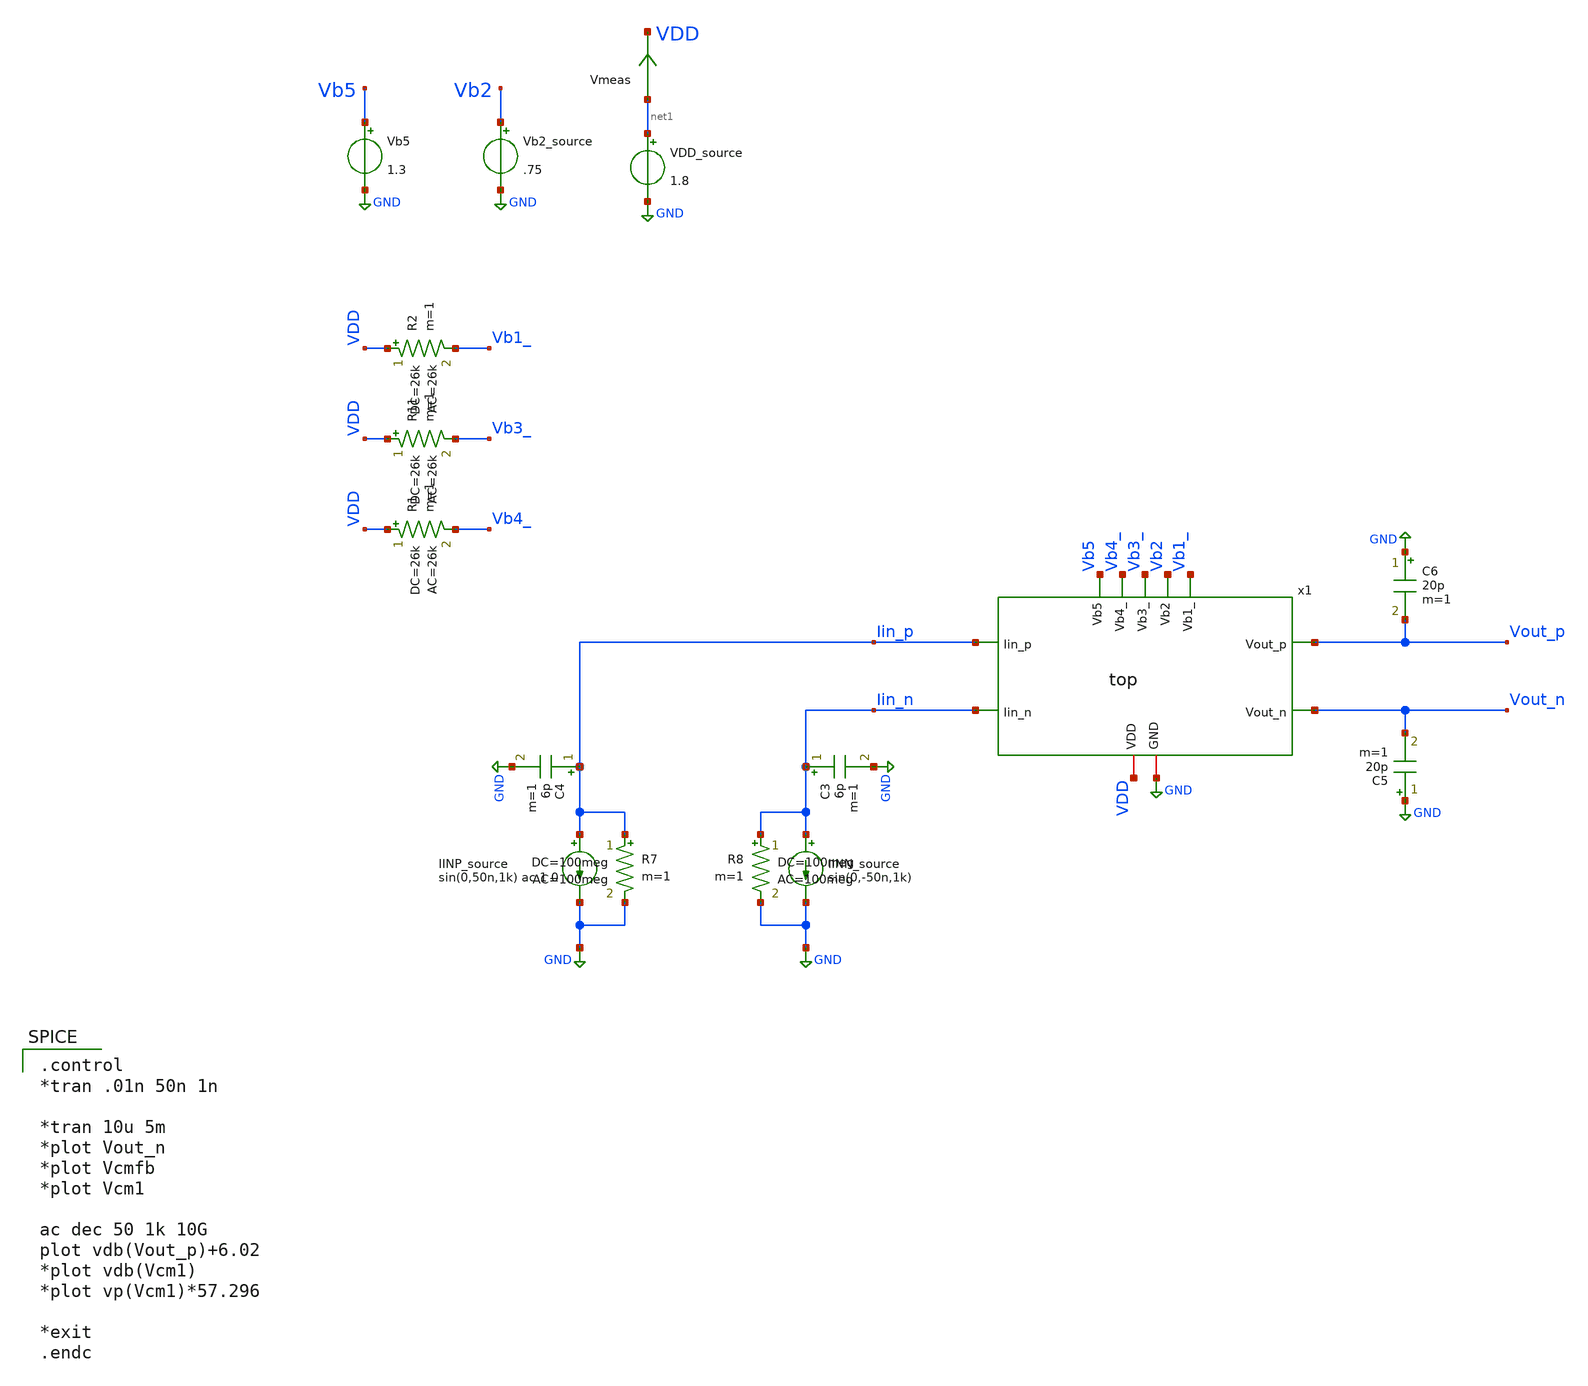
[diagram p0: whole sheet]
** sch_path: xschem/top_tb.sch
**.subckt top_tb
VDD_source net1 GND 1.8
Vmeas net1 VDD 0
.save i(vmeas)
Vb2_source Vb2 GND .75
C3 Iin_n GND 6p m=1
C4 Iin_p GND 6p m=1
IINP_source Iin_p GND sin(0,50n,1k) ac 1 0
IINN_source Iin_n GND sin(0,-50n,1k)
C5 GND Vout_n 20p m=1
C6 GND Vout_p 20p m=1
R7 Iin_p GND 100meg ac=100meg m=1
R8 Iin_n GND 100meg ac=100meg m=1
Vb5 Vb5 GND 1.3
R2 VDD Vb1_ 26k ac=26k m=1
R11 VDD Vb3_ 26k ac=26k m=1
x1 Iin_p Iin_n Vb1_ Vb2 Vb3_ Vb4_ Vb5 VDD GND Vout_n Vout_p top
R1 VDD Vb4_ 26k ac=26k m=1
**** begin user architecture code

.include $::SKYWATER_MODELS/cells/nfet_01v8/sky130_fd_pr__nfet_01v8__tt.corner.spice
.include $::SKYWATER_MODELS/cells/pfet_01v8/sky130_fd_pr__pfet_01v8__tt.corner.spice
.include $::SKYWATER_MODELS/cells/nfet_01v8_lvt/sky130_fd_pr__nfet_01v8_lvt__tt.corner.spice
*.include $::SKYWATER_MODELS/cells/nfet_03v3_nvt/sky130_fd_pr__nfet_03v3_nvt__tt.corner.spice
*.include $::SKYWATER_MODELS/cells/nfet_05v0_nvt/sky130_fd_pr__nfet_05v0_nvt__tt.corner.spice
*.include $::SKYWATER_MODELS/cells/esd_nfet_01v8/sky130_fd_pr__esd_nfet_01v8__tt.corner.spice
*.include $::SKYWATER_MODELS/cells/pfet_01v8_lvt/sky130_fd_pr__pfet_01v8_lvt__tt.corner.spice
*.include $::SKYWATER_MODELS/cells/pfet_01v8_hvt/sky130_fd_pr__pfet_01v8_hvt__tt.corner.spice
*.include $::SKYWATER_MODELS/models/corners/tt/nonfet.spice
* Mismatch parameters
.include $::SKYWATER_MODELS/cells/nfet_01v8/sky130_fd_pr__nfet_01v8__mismatch.corner.spice
.include $::SKYWATER_MODELS/cells/pfet_01v8/sky130_fd_pr__pfet_01v8__mismatch.corner.spice
.include $::SKYWATER_MODELS/cells/nfet_01v8_lvt/sky130_fd_pr__nfet_01v8_lvt__mismatch.corner.spice
*.include $::SKYWATER_MODELS/cells/pfet_01v8_lvt/sky130_fd_pr__pfet_01v8_lvt__mismatch.corner.spice
*.include $::SKYWATER_MODELS/cells/pfet_01v8_hvt/sky130_fd_pr__pfet_01v8_hvt__mismatch.corner.spice
*.include $::SKYWATER_MODELS/cells/nfet_g5v0d10v5/sky130_fd_pr__nfet_g5v0d10v5__mismatch.corner.spice
*.include $::SKYWATER_MODELS/cells/pfet_g5v0d10v5/sky130_fd_pr__pfet_g5v0d10v5__mismatch.corner.spice
*.include $::SKYWATER_MODELS/cells/nfet_05v0_nvt/sky130_fd_pr__nfet_05v0_nvt__mismatch.corner.spice
*.include $::SKYWATER_MODELS/cells/nfet_03v3_nvt/sky130_fd_pr__nfet_03v3_nvt__mismatch.corner.spice
* Resistor$::SKYWATER_MODELS/Capacitor
.include $::SKYWATER_MODELS/models/r+c/res_typical__cap_typical.spice
.include $::SKYWATER_MODELS/models/r+c/res_typical__cap_typical__lin.spice
* Special cells
*.include $::SKYWATER_MODELS/models/corners/tt/specialized_cells.spice
* All models
.include $::SKYWATER_MODELS/models/all.spice
* Corner
*.include $::SKYWATER_MODELS/models/corners/tt/rf.spice
.include /home/jared/Documents/GS_Design/tia_post_approval/pex/top_pex_fixed.spice


.option savecurrents
.control
save all
*NFET

save @m.xm90.msky130_fd_pr__nfet_01v8[vds] @m.xm90.msky130_fd_pr__nfet_01v8[gm]
+ @m.xm90.msky130_fd_pr__nfet_01v8[vth] @m.xm90.msky130_fd_pr__nfet_01v8[vgs] @m.xm90.msky130_fd_pr__nfet_01v8[id]
+ @m.xm90.msky130_fd_pr__nfet_01v8[gds] @m.xm90.msky130_fd_pr__nfet_01v8[cgg] @m.xm90.msky130_fd_pr__nfet_01v8[cgs]
+ @m.xm90.msky130_fd_pr__nfet_01v8[cgd] @m.xm90.msky130_fd_pr__nfet_01v8[cgb] @m.xm90.msky130_fd_pr__nfet_01v8[cdg]
+ @m.xm90.msky130_fd_pr__nfet_01v8[cds] @m.xm90.msky130_fd_pr__nfet_01v8[cdd] @m.xm90.msky130_fd_pr__nfet_01v8[cdb]
+ @m.xm90.msky130_fd_pr__nfet_01v8[csg] @m.xm90.msky130_fd_pr__nfet_01v8[css] @m.xm90.msky130_fd_pr__nfet_01v8[csd]
+ @m.xm90.msky130_fd_pr__nfet_01v8[csb] @m.xm90.msky130_fd_pr__nfet_01v8[cbg] @m.xm90.msky130_fd_pr__nfet_01v8[cbs]
+ @m.xm90.msky130_fd_pr__nfet_01v8[cbd] @m.xm90.msky130_fd_pr__nfet_01v8[cbb]
save @m.xm1.msky130_fd_pr__nfet_01v8[vds] @m.xm1.msky130_fd_pr__nfet_01v8[gm]
+ @m.xm1.msky130_fd_pr__nfet_01v8[vth] @m.xm1.msky130_fd_pr__nfet_01v8[vgs] @m.xm1.msky130_fd_pr__nfet_01v8[id]
+ @m.xm1.msky130_fd_pr__nfet_01v8[gds] @m.xm1.msky130_fd_pr__nfet_01v8[cgg] @m.xm1.msky130_fd_pr__nfet_01v8[cgs]
+ @m.xm1.msky130_fd_pr__nfet_01v8[cgd] @m.xm1.msky130_fd_pr__nfet_01v8[cgb] @m.xm1.msky130_fd_pr__nfet_01v8[cdg]
+ @m.xm1.msky130_fd_pr__nfet_01v8[cds] @m.xm1.msky130_fd_pr__nfet_01v8[cdd] @m.xm1.msky130_fd_pr__nfet_01v8[cdb]
+ @m.xm1.msky130_fd_pr__nfet_01v8[csg] @m.xm1.msky130_fd_pr__nfet_01v8[css] @m.xm1.msky130_fd_pr__nfet_01v8[csd]
+ @m.xm1.msky130_fd_pr__nfet_01v8[csb] @m.xm1.msky130_fd_pr__nfet_01v8[cbg] @m.xm1.msky130_fd_pr__nfet_01v8[cbs]
+ @m.xm1.msky130_fd_pr__nfet_01v8[cbd] @m.xm1.msky130_fd_pr__nfet_01v8[cbb]
save @m.xm2.msky130_fd_pr__nfet_01v8[vds] @m.xm2.msky130_fd_pr__nfet_01v8[gm]
+ @m.xm2.msky130_fd_pr__nfet_01v8[vth] @m.xm2.msky130_fd_pr__nfet_01v8[vgs] @m.xm2.msky130_fd_pr__nfet_01v8[id]
+ @m.xm2.msky130_fd_pr__nfet_01v8[gds] @m.xm2.msky130_fd_pr__nfet_01v8[cgg] @m.xm2.msky130_fd_pr__nfet_01v8[cgs]
+ @m.xm2.msky130_fd_pr__nfet_01v8[cgd] @m.xm2.msky130_fd_pr__nfet_01v8[cgb] @m.xm2.msky130_fd_pr__nfet_01v8[cdg]
+ @m.xm2.msky130_fd_pr__nfet_01v8[cds] @m.xm2.msky130_fd_pr__nfet_01v8[cdd] @m.xm2.msky130_fd_pr__nfet_01v8[cdb]
+ @m.xm2.msky130_fd_pr__nfet_01v8[csg] @m.xm2.msky130_fd_pr__nfet_01v8[css] @m.xm2.msky130_fd_pr__nfet_01v8[csd]
+ @m.xm2.msky130_fd_pr__nfet_01v8[csb] @m.xm2.msky130_fd_pr__nfet_01v8[cbg] @m.xm2.msky130_fd_pr__nfet_01v8[cbs]
+ @m.xm2.msky130_fd_pr__nfet_01v8[cbd] @m.xm2.msky130_fd_pr__nfet_01v8[cbb]
save @m.xm3.msky130_fd_pr__nfet_01v8[vds] @m.xm3.msky130_fd_pr__nfet_01v8[gm]
+ @m.xm3.msky130_fd_pr__nfet_01v8[vth] @m.xm3.msky130_fd_pr__nfet_01v8[vgs] @m.xm3.msky130_fd_pr__nfet_01v8[id]
+ @m.xm3.msky130_fd_pr__nfet_01v8[gds] @m.xm3.msky130_fd_pr__nfet_01v8[cgg] @m.xm3.msky130_fd_pr__nfet_01v8[cgs]
+ @m.xm3.msky130_fd_pr__nfet_01v8[cgd] @m.xm3.msky130_fd_pr__nfet_01v8[cgb] @m.xm3.msky130_fd_pr__nfet_01v8[cdg]
+ @m.xm3.msky130_fd_pr__nfet_01v8[cds] @m.xm3.msky130_fd_pr__nfet_01v8[cdd] @m.xm3.msky130_fd_pr__nfet_01v8[cdb]
+ @m.xm3.msky130_fd_pr__nfet_01v8[csg] @m.xm3.msky130_fd_pr__nfet_01v8[css] @m.xm3.msky130_fd_pr__nfet_01v8[csd]
+ @m.xm3.msky130_fd_pr__nfet_01v8[csb] @m.xm3.msky130_fd_pr__nfet_01v8[cbg] @m.xm3.msky130_fd_pr__nfet_01v8[cbs]
+ @m.xm3.msky130_fd_pr__nfet_01v8[cbd] @m.xm3.msky130_fd_pr__nfet_01v8[cbb]
save @m.xm6.msky130_fd_pr__nfet_01v8[vds] @m.xm6.msky130_fd_pr__nfet_01v8[gm]
+ @m.xm6.msky130_fd_pr__nfet_01v8[vth] @m.xm6.msky130_fd_pr__nfet_01v8[vgs] @m.xm6.msky130_fd_pr__nfet_01v8[id]
+ @m.xm6.msky130_fd_pr__nfet_01v8[gds] @m.xm6.msky130_fd_pr__nfet_01v8[cgg] @m.xm6.msky130_fd_pr__nfet_01v8[cgs]
+ @m.xm6.msky130_fd_pr__nfet_01v8[cgd] @m.xm6.msky130_fd_pr__nfet_01v8[cgb] @m.xm6.msky130_fd_pr__nfet_01v8[cdg]
+ @m.xm6.msky130_fd_pr__nfet_01v8[cds] @m.xm6.msky130_fd_pr__nfet_01v8[cdd] @m.xm6.msky130_fd_pr__nfet_01v8[cdb]
+ @m.xm6.msky130_fd_pr__nfet_01v8[csg] @m.xm6.msky130_fd_pr__nfet_01v8[css] @m.xm6.msky130_fd_pr__nfet_01v8[csd]
+ @m.xm6.msky130_fd_pr__nfet_01v8[csb] @m.xm6.msky130_fd_pr__nfet_01v8[cbg] @m.xm6.msky130_fd_pr__nfet_01v8[cbs]
+ @m.xm6.msky130_fd_pr__nfet_01v8[cbd] @m.xm6.msky130_fd_pr__nfet_01v8[cbb]
save @m.xm7.msky130_fd_pr__nfet_01v8[vds] @m.xm7.msky130_fd_pr__nfet_01v8[gm]
+ @m.xm7.msky130_fd_pr__nfet_01v8[vth] @m.xm7.msky130_fd_pr__nfet_01v8[vgs] @m.xm7.msky130_fd_pr__nfet_01v8[id]
+ @m.xm7.msky130_fd_pr__nfet_01v8[gds] @m.xm7.msky130_fd_pr__nfet_01v8[cgg] @m.xm7.msky130_fd_pr__nfet_01v8[cgs]
+ @m.xm7.msky130_fd_pr__nfet_01v8[cgd] @m.xm7.msky130_fd_pr__nfet_01v8[cgb] @m.xm7.msky130_fd_pr__nfet_01v8[cdg]
+ @m.xm7.msky130_fd_pr__nfet_01v8[cds] @m.xm7.msky130_fd_pr__nfet_01v8[cdd] @m.xm7.msky130_fd_pr__nfet_01v8[cdb]
+ @m.xm7.msky130_fd_pr__nfet_01v8[csg] @m.xm7.msky130_fd_pr__nfet_01v8[css] @m.xm7.msky130_fd_pr__nfet_01v8[csd]
+ @m.xm7.msky130_fd_pr__nfet_01v8[csb] @m.xm7.msky130_fd_pr__nfet_01v8[cbg] @m.xm7.msky130_fd_pr__nfet_01v8[cbs]
+ @m.xm7.msky130_fd_pr__nfet_01v8[cbd] @m.xm7.msky130_fd_pr__nfet_01v8[cbb]
save @m.xm8.msky130_fd_pr__nfet_01v8[vds] @m.xm8.msky130_fd_pr__nfet_01v8[gm]
+ @m.xm8.msky130_fd_pr__nfet_01v8[vth] @m.xm8.msky130_fd_pr__nfet_01v8[vgs] @m.xm8.msky130_fd_pr__nfet_01v8[id]
+ @m.xm8.msky130_fd_pr__nfet_01v8[gds] @m.xm8.msky130_fd_pr__nfet_01v8[cgg] @m.xm8.msky130_fd_pr__nfet_01v8[cgs]
+ @m.xm8.msky130_fd_pr__nfet_01v8[cgd] @m.xm8.msky130_fd_pr__nfet_01v8[cgb] @m.xm8.msky130_fd_pr__nfet_01v8[cdg]
+ @m.xm8.msky130_fd_pr__nfet_01v8[cds] @m.xm8.msky130_fd_pr__nfet_01v8[cdd] @m.xm8.msky130_fd_pr__nfet_01v8[cdb]
+ @m.xm8.msky130_fd_pr__nfet_01v8[csg] @m.xm8.msky130_fd_pr__nfet_01v8[css] @m.xm8.msky130_fd_pr__nfet_01v8[csd]
+ @m.xm8.msky130_fd_pr__nfet_01v8[csb] @m.xm8.msky130_fd_pr__nfet_01v8[cbg] @m.xm8.msky130_fd_pr__nfet_01v8[cbs]
+ @m.xm8.msky130_fd_pr__nfet_01v8[cbd] @m.xm8.msky130_fd_pr__nfet_01v8[cbb]
save @m.xm11.msky130_fd_pr__nfet_01v8[vds] @m.xm11.msky130_fd_pr__nfet_01v8[gm]
+ @m.xm11.msky130_fd_pr__nfet_01v8[vth] @m.xm11.msky130_fd_pr__nfet_01v8[vgs] @m.xm11.msky130_fd_pr__nfet_01v8[id]
+ @m.xm11.msky130_fd_pr__nfet_01v8[gds] @m.xm11.msky130_fd_pr__nfet_01v8[cgg] @m.xm11.msky130_fd_pr__nfet_01v8[cgs]
+ @m.xm11.msky130_fd_pr__nfet_01v8[cgd] @m.xm11.msky130_fd_pr__nfet_01v8[cgb] @m.xm11.msky130_fd_pr__nfet_01v8[cdg]
+ @m.xm11.msky130_fd_pr__nfet_01v8[cds] @m.xm11.msky130_fd_pr__nfet_01v8[cdd] @m.xm11.msky130_fd_pr__nfet_01v8[cdb]
+ @m.xm11.msky130_fd_pr__nfet_01v8[csg] @m.xm11.msky130_fd_pr__nfet_01v8[css] @m.xm11.msky130_fd_pr__nfet_01v8[csd]
+ @m.xm11.msky130_fd_pr__nfet_01v8[csb] @m.xm11.msky130_fd_pr__nfet_01v8[cbg] @m.xm11.msky130_fd_pr__nfet_01v8[cbs]
+ @m.xm11.msky130_fd_pr__nfet_01v8[cbd] @m.xm11.msky130_fd_pr__nfet_01v8[cbb]
save @m.xm12.msky130_fd_pr__nfet_01v8[vds] @m.xm12.msky130_fd_pr__nfet_01v8[gm]
+ @m.xm12.msky130_fd_pr__nfet_01v8[vth] @m.xm12.msky130_fd_pr__nfet_01v8[vgs] @m.xm12.msky130_fd_pr__nfet_01v8[id]
+ @m.xm12.msky130_fd_pr__nfet_01v8[gds] @m.xm12.msky130_fd_pr__nfet_01v8[cgg] @m.xm12.msky130_fd_pr__nfet_01v8[cgs]
+ @m.xm12.msky130_fd_pr__nfet_01v8[cgd] @m.xm12.msky130_fd_pr__nfet_01v8[cgb] @m.xm12.msky130_fd_pr__nfet_01v8[cdg]
+ @m.xm12.msky130_fd_pr__nfet_01v8[cds] @m.xm12.msky130_fd_pr__nfet_01v8[cdd] @m.xm12.msky130_fd_pr__nfet_01v8[cdb]
+ @m.xm12.msky130_fd_pr__nfet_01v8[csg] @m.xm12.msky130_fd_pr__nfet_01v8[css] @m.xm12.msky130_fd_pr__nfet_01v8[csd]
+ @m.xm12.msky130_fd_pr__nfet_01v8[csb] @m.xm12.msky130_fd_pr__nfet_01v8[cbg] @m.xm12.msky130_fd_pr__nfet_01v8[cbs]
+ @m.xm12.msky130_fd_pr__nfet_01v8[cbd] @m.xm12.msky130_fd_pr__nfet_01v8[cbb]
save @m.xm16.msky130_fd_pr__nfet_01v8[vds] @m.xm16.msky130_fd_pr__nfet_01v8[gm]
+ @m.xm16.msky130_fd_pr__nfet_01v8[vth] @m.xm16.msky130_fd_pr__nfet_01v8[vgs] @m.xm16.msky130_fd_pr__nfet_01v8[id]
+ @m.xm16.msky130_fd_pr__nfet_01v8[gds] @m.xm16.msky130_fd_pr__nfet_01v8[cgg] @m.xm16.msky130_fd_pr__nfet_01v8[cgs]
+ @m.xm16.msky130_fd_pr__nfet_01v8[cgd] @m.xm16.msky130_fd_pr__nfet_01v8[cgb] @m.xm16.msky130_fd_pr__nfet_01v8[cdg]
+ @m.xm16.msky130_fd_pr__nfet_01v8[cds] @m.xm16.msky130_fd_pr__nfet_01v8[cdd] @m.xm16.msky130_fd_pr__nfet_01v8[cdb]
+ @m.xm16.msky130_fd_pr__nfet_01v8[csg] @m.xm16.msky130_fd_pr__nfet_01v8[css] @m.xm16.msky130_fd_pr__nfet_01v8[csd]
+ @m.xm16.msky130_fd_pr__nfet_01v8[csb] @m.xm16.msky130_fd_pr__nfet_01v8[cbg] @m.xm16.msky130_fd_pr__nfet_01v8[cbs]
+ @m.xm16.msky130_fd_pr__nfet_01v8[cbd] @m.xm16.msky130_fd_pr__nfet_01v8[cbb]
save @m.xm17.msky130_fd_pr__nfet_01v8_lvt[vds] @m.xm17.msky130_fd_pr__nfet_01v8_lvt[gm]
+ @m.xm17.msky130_fd_pr__nfet_01v8_lvt[vth] @m.xm17.msky130_fd_pr__nfet_01v8_lvt[vgs] @m.xm17.msky130_fd_pr__nfet_01v8_lvt[id]
+ @m.xm17.msky130_fd_pr__nfet_01v8_lvt[gds] @m.xm17.msky130_fd_pr__nfet_01v8_lvt[cgg] @m.xm17.msky130_fd_pr__nfet_01v8_lvt[cgs]
+ @m.xm17.msky130_fd_pr__nfet_01v8_lvt[cgd] @m.xm17.msky130_fd_pr__nfet_01v8_lvt[cgb] @m.xm17.msky130_fd_pr__nfet_01v8_lvt[cdg]
+ @m.xm17.msky130_fd_pr__nfet_01v8_lvt[cds] @m.xm17.msky130_fd_pr__nfet_01v8_lvt[cdd] @m.xm17.msky130_fd_pr__nfet_01v8_lvt[cdb]
+ @m.xm17.msky130_fd_pr__nfet_01v8_lvt[csg] @m.xm17.msky130_fd_pr__nfet_01v8_lvt[css] @m.xm17.msky130_fd_pr__nfet_01v8_lvt[csd]
+ @m.xm17.msky130_fd_pr__nfet_01v8_lvt[csb] @m.xm17.msky130_fd_pr__nfet_01v8_lvt[cbg] @m.xm17.msky130_fd_pr__nfet_01v8_lvt[cbs]
+ @m.xm17.msky130_fd_pr__nfet_01v8_lvt[cbd] @m.xm17.msky130_fd_pr__nfet_01v8_lvt[cbb]
save @m.xm18.msky130_fd_pr__nfet_01v8_lvt[vds] @m.xm18.msky130_fd_pr__nfet_01v8_lvt[gm]
+ @m.xm18.msky130_fd_pr__nfet_01v8_lvt[vth] @m.xm18.msky130_fd_pr__nfet_01v8_lvt[vgs] @m.xm18.msky130_fd_pr__nfet_01v8_lvt[id]
+ @m.xm18.msky130_fd_pr__nfet_01v8_lvt[gds] @m.xm18.msky130_fd_pr__nfet_01v8_lvt[cgg] @m.xm18.msky130_fd_pr__nfet_01v8_lvt[cgs]
+ @m.xm18.msky130_fd_pr__nfet_01v8_lvt[cgd] @m.xm18.msky130_fd_pr__nfet_01v8_lvt[cgb] @m.xm18.msky130_fd_pr__nfet_01v8_lvt[cdg]
+ @m.xm18.msky130_fd_pr__nfet_01v8_lvt[cds] @m.xm18.msky130_fd_pr__nfet_01v8_lvt[cdd] @m.xm18.msky130_fd_pr__nfet_01v8_lvt[cdb]
+ @m.xm18.msky130_fd_pr__nfet_01v8_lvt[csg] @m.xm18.msky130_fd_pr__nfet_01v8_lvt[css] @m.xm18.msky130_fd_pr__nfet_01v8_lvt[csd]
+ @m.xm18.msky130_fd_pr__nfet_01v8_lvt[csb] @m.xm18.msky130_fd_pr__nfet_01v8_lvt[cbg] @m.xm18.msky130_fd_pr__nfet_01v8_lvt[cbs]
+ @m.xm18.msky130_fd_pr__nfet_01v8_lvt[cbd] @m.xm18.msky130_fd_pr__nfet_01v8_lvt[cbb]
save @m.xm19.msky130_fd_pr__nfet_01v8[vds] @m.xm19.msky130_fd_pr__nfet_01v8[gm]
+ @m.xm19.msky130_fd_pr__nfet_01v8[vth] @m.xm19.msky130_fd_pr__nfet_01v8[vgs] @m.xm19.msky130_fd_pr__nfet_01v8[id]
+ @m.xm19.msky130_fd_pr__nfet_01v8[gds] @m.xm19.msky130_fd_pr__nfet_01v8[cgg] @m.xm19.msky130_fd_pr__nfet_01v8[cgs]
+ @m.xm19.msky130_fd_pr__nfet_01v8[cgd] @m.xm19.msky130_fd_pr__nfet_01v8[cgb] @m.xm19.msky130_fd_pr__nfet_01v8[cdg]
+ @m.xm19.msky130_fd_pr__nfet_01v8[cds] @m.xm19.msky130_fd_pr__nfet_01v8[cdd] @m.xm19.msky130_fd_pr__nfet_01v8[cdb]
+ @m.xm19.msky130_fd_pr__nfet_01v8[csg] @m.xm19.msky130_fd_pr__nfet_01v8[css] @m.xm19.msky130_fd_pr__nfet_01v8[csd]
+ @m.xm19.msky130_fd_pr__nfet_01v8[csb] @m.xm19.msky130_fd_pr__nfet_01v8[cbg] @m.xm19.msky130_fd_pr__nfet_01v8[cbs]
+ @m.xm19.msky130_fd_pr__nfet_01v8[cbd] @m.xm19.msky130_fd_pr__nfet_01v8[cbb]
save @m.xm30.msky130_fd_pr__nfet_01v8[vds] @m.xm30.msky130_fd_pr__nfet_01v8[gm]
+ @m.xm30.msky130_fd_pr__nfet_01v8[vth] @m.xm30.msky130_fd_pr__nfet_01v8[vgs] @m.xm30.msky130_fd_pr__nfet_01v8[id]
+ @m.xm30.msky130_fd_pr__nfet_01v8[gds] @m.xm30.msky130_fd_pr__nfet_01v8[cgg] @m.xm30.msky130_fd_pr__nfet_01v8[cgs]
+ @m.xm30.msky130_fd_pr__nfet_01v8[cgd] @m.xm30.msky130_fd_pr__nfet_01v8[cgb] @m.xm30.msky130_fd_pr__nfet_01v8[cdg]
+ @m.xm30.msky130_fd_pr__nfet_01v8[cds] @m.xm30.msky130_fd_pr__nfet_01v8[cdd] @m.xm30.msky130_fd_pr__nfet_01v8[cdb]
+ @m.xm30.msky130_fd_pr__nfet_01v8[csg] @m.xm30.msky130_fd_pr__nfet_01v8[css] @m.xm30.msky130_fd_pr__nfet_01v8[csd]
+ @m.xm30.msky130_fd_pr__nfet_01v8[csb] @m.xm30.msky130_fd_pr__nfet_01v8[cbg] @m.xm30.msky130_fd_pr__nfet_01v8[cbs]
+ @m.xm30.msky130_fd_pr__nfet_01v8[cbd] @m.xm30.msky130_fd_pr__nfet_01v8[cbb]
save @m.xm26.msky130_fd_pr__nfet_01v8[vds] @m.xm26.msky130_fd_pr__nfet_01v8[gm]
+ @m.xm26.msky130_fd_pr__nfet_01v8[vth] @m.xm26.msky130_fd_pr__nfet_01v8[vgs] @m.xm26.msky130_fd_pr__nfet_01v8[id]
+ @m.xm26.msky130_fd_pr__nfet_01v8[gds] @m.xm26.msky130_fd_pr__nfet_01v8[cgg] @m.xm26.msky130_fd_pr__nfet_01v8[cgs]
+ @m.xm26.msky130_fd_pr__nfet_01v8[cgd] @m.xm26.msky130_fd_pr__nfet_01v8[cgb] @m.xm26.msky130_fd_pr__nfet_01v8[cdg]
+ @m.xm26.msky130_fd_pr__nfet_01v8[cds] @m.xm26.msky130_fd_pr__nfet_01v8[cdd] @m.xm26.msky130_fd_pr__nfet_01v8[cdb]
+ @m.xm26.msky130_fd_pr__nfet_01v8[csg] @m.xm26.msky130_fd_pr__nfet_01v8[css] @m.xm26.msky130_fd_pr__nfet_01v8[csd]
+ @m.xm26.msky130_fd_pr__nfet_01v8[csb] @m.xm26.msky130_fd_pr__nfet_01v8[cbg] @m.xm26.msky130_fd_pr__nfet_01v8[cbs]
+ @m.xm26.msky130_fd_pr__nfet_01v8[cbd] @m.xm26.msky130_fd_pr__nfet_01v8[cbb]
save @m.xm27.msky130_fd_pr__nfet_01v8[vds] @m.xm27.msky130_fd_pr__nfet_01v8[gm]
+ @m.xm27.msky130_fd_pr__nfet_01v8[vth] @m.xm27.msky130_fd_pr__nfet_01v8[vgs] @m.xm27.msky130_fd_pr__nfet_01v8[id]
+ @m.xm27.msky130_fd_pr__nfet_01v8[gds] @m.xm27.msky130_fd_pr__nfet_01v8[cgg] @m.xm27.msky130_fd_pr__nfet_01v8[cgs]
+ @m.xm27.msky130_fd_pr__nfet_01v8[cgd] @m.xm27.msky130_fd_pr__nfet_01v8[cgb] @m.xm27.msky130_fd_pr__nfet_01v8[cdg]
+ @m.xm27.msky130_fd_pr__nfet_01v8[cds] @m.xm27.msky130_fd_pr__nfet_01v8[cdd] @m.xm27.msky130_fd_pr__nfet_01v8[cdb]
+ @m.xm27.msky130_fd_pr__nfet_01v8[csg] @m.xm27.msky130_fd_pr__nfet_01v8[css] @m.xm27.msky130_fd_pr__nfet_01v8[csd]
+ @m.xm27.msky130_fd_pr__nfet_01v8[csb] @m.xm27.msky130_fd_pr__nfet_01v8[cbg] @m.xm27.msky130_fd_pr__nfet_01v8[cbs]
+ @m.xm27.msky130_fd_pr__nfet_01v8[cbd] @m.xm27.msky130_fd_pr__nfet_01v8[cbb]

*PFET

save @m.xm91.msky130_fd_pr__pfet_01v8[vds] @m.xm91.msky130_fd_pr__pfet_01v8[gm]
+ @m.xm91.msky130_fd_pr__pfet_01v8[vth] @m.xm91.msky130_fd_pr__pfet_01v8[vgs] @m.xm91.msky130_fd_pr__pfet_01v8[id]
+ @m.xm91.msky130_fd_pr__pfet_01v8[gds] @m.xm91.msky130_fd_pr__pfet_01v8[cgg] @m.xm91.msky130_fd_pr__pfet_01v8[cgs]
+ @m.xm91.msky130_fd_pr__pfet_01v8[cgd] @m.xm91.msky130_fd_pr__pfet_01v8[cgb] @m.xm91.msky130_fd_pr__pfet_01v8[cdg]
+ @m.xm91.msky130_fd_pr__pfet_01v8[cds] @m.xm91.msky130_fd_pr__pfet_01v8[cdd] @m.xm91.msky130_fd_pr__pfet_01v8[cdb]
+ @m.xm91.msky130_fd_pr__pfet_01v8[csg] @m.xm91.msky130_fd_pr__pfet_01v8[css] @m.xm91.msky130_fd_pr__pfet_01v8[csd]
+ @m.xm91.msky130_fd_pr__pfet_01v8[csb] @m.xm91.msky130_fd_pr__pfet_01v8[cbg] @m.xm91.msky130_fd_pr__pfet_01v8[cbs]
+ @m.xm91.msky130_fd_pr__pfet_01v8[cbd] @m.xm91.msky130_fd_pr__pfet_01v8[cbb]
save @m.xm4.msky130_fd_pr__pfet_01v8[vds] @m.xm4.msky130_fd_pr__pfet_01v8[gm]
+ @m.xm4.msky130_fd_pr__pfet_01v8[vth] @m.xm4.msky130_fd_pr__pfet_01v8[vgs] @m.xm4.msky130_fd_pr__pfet_01v8[id]
+ @m.xm4.msky130_fd_pr__pfet_01v8[gds] @m.xm4.msky130_fd_pr__pfet_01v8[cgg] @m.xm4.msky130_fd_pr__pfet_01v8[cgs]
+ @m.xm4.msky130_fd_pr__pfet_01v8[cgd] @m.xm4.msky130_fd_pr__pfet_01v8[cgb] @m.xm4.msky130_fd_pr__pfet_01v8[cdg]
+ @m.xm4.msky130_fd_pr__pfet_01v8[cds] @m.xm4.msky130_fd_pr__pfet_01v8[cdd] @m.xm4.msky130_fd_pr__pfet_01v8[cdb]
+ @m.xm4.msky130_fd_pr__pfet_01v8[csg] @m.xm4.msky130_fd_pr__pfet_01v8[css] @m.xm4.msky130_fd_pr__pfet_01v8[csd]
+ @m.xm4.msky130_fd_pr__pfet_01v8[csb] @m.xm4.msky130_fd_pr__pfet_01v8[cbg] @m.xm4.msky130_fd_pr__pfet_01v8[cbs]
+ @m.xm4.msky130_fd_pr__pfet_01v8[cbd] @m.xm4.msky130_fd_pr__pfet_01v8[cbb]
save @m.xm5.msky130_fd_pr__pfet_01v8[vds] @m.xm5.msky130_fd_pr__pfet_01v8[gm]
+ @m.xm5.msky130_fd_pr__pfet_01v8[vth] @m.xm5.msky130_fd_pr__pfet_01v8[vgs] @m.xm5.msky130_fd_pr__pfet_01v8[id]
+ @m.xm5.msky130_fd_pr__pfet_01v8[gds] @m.xm5.msky130_fd_pr__pfet_01v8[cgg] @m.xm5.msky130_fd_pr__pfet_01v8[cgs]
+ @m.xm5.msky130_fd_pr__pfet_01v8[cgd] @m.xm5.msky130_fd_pr__pfet_01v8[cgb] @m.xm5.msky130_fd_pr__pfet_01v8[cdg]
+ @m.xm5.msky130_fd_pr__pfet_01v8[cds] @m.xm5.msky130_fd_pr__pfet_01v8[cdd] @m.xm5.msky130_fd_pr__pfet_01v8[cdb]
+ @m.xm5.msky130_fd_pr__pfet_01v8[csg] @m.xm5.msky130_fd_pr__pfet_01v8[css] @m.xm5.msky130_fd_pr__pfet_01v8[csd]
+ @m.xm5.msky130_fd_pr__pfet_01v8[csb] @m.xm5.msky130_fd_pr__pfet_01v8[cbg] @m.xm5.msky130_fd_pr__pfet_01v8[cbs]
+ @m.xm5.msky130_fd_pr__pfet_01v8[cbd] @m.xm5.msky130_fd_pr__pfet_01v8[cbb]
save @m.xm9.msky130_fd_pr__pfet_01v8[vds] @m.xm9.msky130_fd_pr__pfet_01v8[gm]
+ @m.xm9.msky130_fd_pr__pfet_01v8[vth] @m.xm9.msky130_fd_pr__pfet_01v8[vgs] @m.xm9.msky130_fd_pr__pfet_01v8[id]
+ @m.xm9.msky130_fd_pr__pfet_01v8[gds] @m.xm9.msky130_fd_pr__pfet_01v8[cgg] @m.xm9.msky130_fd_pr__pfet_01v8[cgs]
+ @m.xm9.msky130_fd_pr__pfet_01v8[cgd] @m.xm9.msky130_fd_pr__pfet_01v8[cgb] @m.xm9.msky130_fd_pr__pfet_01v8[cdg]
+ @m.xm9.msky130_fd_pr__pfet_01v8[cds] @m.xm9.msky130_fd_pr__pfet_01v8[cdd] @m.xm9.msky130_fd_pr__pfet_01v8[cdb]
+ @m.xm9.msky130_fd_pr__pfet_01v8[csg] @m.xm9.msky130_fd_pr__pfet_01v8[css] @m.xm9.msky130_fd_pr__pfet_01v8[csd]
+ @m.xm9.msky130_fd_pr__pfet_01v8[csb] @m.xm9.msky130_fd_pr__pfet_01v8[cbg] @m.xm9.msky130_fd_pr__pfet_01v8[cbs]
+ @m.xm9.msky130_fd_pr__pfet_01v8[cbd] @m.xm9.msky130_fd_pr__pfet_01v8[cbb]
save @m.xm10.msky130_fd_pr__pfet_01v8[vds] @m.xm10.msky130_fd_pr__pfet_01v8[gm]
+ @m.xm10.msky130_fd_pr__pfet_01v8[vth] @m.xm10.msky130_fd_pr__pfet_01v8[vgs] @m.xm10.msky130_fd_pr__pfet_01v8[id]
+ @m.xm10.msky130_fd_pr__pfet_01v8[gds] @m.xm10.msky130_fd_pr__pfet_01v8[cgg] @m.xm10.msky130_fd_pr__pfet_01v8[cgs]
+ @m.xm10.msky130_fd_pr__pfet_01v8[cgd] @m.xm10.msky130_fd_pr__pfet_01v8[cgb] @m.xm10.msky130_fd_pr__pfet_01v8[cdg]
+ @m.xm10.msky130_fd_pr__pfet_01v8[cds] @m.xm10.msky130_fd_pr__pfet_01v8[cdd] @m.xm10.msky130_fd_pr__pfet_01v8[cdb]
+ @m.xm10.msky130_fd_pr__pfet_01v8[csg] @m.xm10.msky130_fd_pr__pfet_01v8[css] @m.xm10.msky130_fd_pr__pfet_01v8[csd]
+ @m.xm10.msky130_fd_pr__pfet_01v8[csb] @m.xm10.msky130_fd_pr__pfet_01v8[cbg] @m.xm10.msky130_fd_pr__pfet_01v8[cbs]
+ @m.xm10.msky130_fd_pr__pfet_01v8[cbd] @m.xm10.msky130_fd_pr__pfet_01v8[cbb]
save @m.xm13.msky130_fd_pr__pfet_01v8[vds] @m.xm13.msky130_fd_pr__pfet_01v8[gm]
+ @m.xm13.msky130_fd_pr__pfet_01v8[vth] @m.xm13.msky130_fd_pr__pfet_01v8[vgs] @m.xm13.msky130_fd_pr__pfet_01v8[id]
+ @m.xm13.msky130_fd_pr__pfet_01v8[gds] @m.xm13.msky130_fd_pr__pfet_01v8[cgg] @m.xm13.msky130_fd_pr__pfet_01v8[cgs]
+ @m.xm13.msky130_fd_pr__pfet_01v8[cgd] @m.xm13.msky130_fd_pr__pfet_01v8[cgb] @m.xm13.msky130_fd_pr__pfet_01v8[cdg]
+ @m.xm13.msky130_fd_pr__pfet_01v8[cds] @m.xm13.msky130_fd_pr__pfet_01v8[cdd] @m.xm13.msky130_fd_pr__pfet_01v8[cdb]
+ @m.xm13.msky130_fd_pr__pfet_01v8[csg] @m.xm13.msky130_fd_pr__pfet_01v8[css] @m.xm13.msky130_fd_pr__pfet_01v8[csd]
+ @m.xm13.msky130_fd_pr__pfet_01v8[csb] @m.xm13.msky130_fd_pr__pfet_01v8[cbg] @m.xm13.msky130_fd_pr__pfet_01v8[cbs]
+ @m.xm13.msky130_fd_pr__pfet_01v8[cbd] @m.xm13.msky130_fd_pr__pfet_01v8[cbb]
save @m.xm14.msky130_fd_pr__pfet_01v8[vds] @m.xm14.msky130_fd_pr__pfet_01v8[gm]
+ @m.xm14.msky130_fd_pr__pfet_01v8[vth] @m.xm14.msky130_fd_pr__pfet_01v8[vgs] @m.xm14.msky130_fd_pr__pfet_01v8[id]
+ @m.xm14.msky130_fd_pr__pfet_01v8[gds] @m.xm14.msky130_fd_pr__pfet_01v8[cgg] @m.xm14.msky130_fd_pr__pfet_01v8[cgs]
+ @m.xm14.msky130_fd_pr__pfet_01v8[cgd] @m.xm14.msky130_fd_pr__pfet_01v8[cgb] @m.xm14.msky130_fd_pr__pfet_01v8[cdg]
+ @m.xm14.msky130_fd_pr__pfet_01v8[cds] @m.xm14.msky130_fd_pr__pfet_01v8[cdd] @m.xm14.msky130_fd_pr__pfet_01v8[cdb]
+ @m.xm14.msky130_fd_pr__pfet_01v8[csg] @m.xm14.msky130_fd_pr__pfet_01v8[css] @m.xm14.msky130_fd_pr__pfet_01v8[csd]
+ @m.xm14.msky130_fd_pr__pfet_01v8[csb] @m.xm14.msky130_fd_pr__pfet_01v8[cbg] @m.xm14.msky130_fd_pr__pfet_01v8[cbs]
+ @m.xm14.msky130_fd_pr__pfet_01v8[cbd] @m.xm14.msky130_fd_pr__pfet_01v8[cbb]
save @m.xm24.msky130_fd_pr__pfet_01v8[vds] @m.xm24.msky130_fd_pr__pfet_01v8[gm]
+ @m.xm24.msky130_fd_pr__pfet_01v8[vth] @m.xm24.msky130_fd_pr__pfet_01v8[vgs] @m.xm24.msky130_fd_pr__pfet_01v8[id]
+ @m.xm24.msky130_fd_pr__pfet_01v8[gds] @m.xm24.msky130_fd_pr__pfet_01v8[cgg] @m.xm24.msky130_fd_pr__pfet_01v8[cgs]
+ @m.xm24.msky130_fd_pr__pfet_01v8[cgd] @m.xm24.msky130_fd_pr__pfet_01v8[cgb] @m.xm24.msky130_fd_pr__pfet_01v8[cdg]
+ @m.xm24.msky130_fd_pr__pfet_01v8[cds] @m.xm24.msky130_fd_pr__pfet_01v8[cdd] @m.xm24.msky130_fd_pr__pfet_01v8[cdb]
+ @m.xm24.msky130_fd_pr__pfet_01v8[csg] @m.xm24.msky130_fd_pr__pfet_01v8[css] @m.xm24.msky130_fd_pr__pfet_01v8[csd]
+ @m.xm24.msky130_fd_pr__pfet_01v8[csb] @m.xm24.msky130_fd_pr__pfet_01v8[cbg] @m.xm24.msky130_fd_pr__pfet_01v8[cbs]
+ @m.xm24.msky130_fd_pr__pfet_01v8[cbd] @m.xm24.msky130_fd_pr__pfet_01v8[cbb]
save @m.xm25.msky130_fd_pr__pfet_01v8[vds] @m.xm25.msky130_fd_pr__pfet_01v8[gm]
+ @m.xm25.msky130_fd_pr__pfet_01v8[vth] @m.xm25.msky130_fd_pr__pfet_01v8[vgs] @m.xm25.msky130_fd_pr__pfet_01v8[id]
+ @m.xm25.msky130_fd_pr__pfet_01v8[gds] @m.xm25.msky130_fd_pr__pfet_01v8[cgg] @m.xm25.msky130_fd_pr__pfet_01v8[cgs]
+ @m.xm25.msky130_fd_pr__pfet_01v8[cgd] @m.xm25.msky130_fd_pr__pfet_01v8[cgb] @m.xm25.msky130_fd_pr__pfet_01v8[cdg]
+ @m.xm25.msky130_fd_pr__pfet_01v8[cds] @m.xm25.msky130_fd_pr__pfet_01v8[cdd] @m.xm25.msky130_fd_pr__pfet_01v8[cdb]
+ @m.xm25.msky130_fd_pr__pfet_01v8[csg] @m.xm25.msky130_fd_pr__pfet_01v8[css] @m.xm25.msky130_fd_pr__pfet_01v8[csd]
+ @m.xm25.msky130_fd_pr__pfet_01v8[csb] @m.xm25.msky130_fd_pr__pfet_01v8[cbg] @m.xm25.msky130_fd_pr__pfet_01v8[cbs]
+ @m.xm25.msky130_fd_pr__pfet_01v8[cbd] @m.xm25.msky130_fd_pr__pfet_01v8[cbb]

op
write top_tb.raw
.endc


.control
*tran .01n 50n 1n

*tran 10u 5m
*plot Vout_n
*plot Vcmfb
*plot Vcm1

ac dec 50 1k 10G
plot vdb(Vout_p)+6.02
*plot vdb(Vcm1)
*plot vp(Vcm1)*57.296

*exit
.endc


**** end user architecture code
**.ends

* expanding   symbol:  tia_post_approval/schem/top.sym # of pins=11
** sym_path: tia_post_approval/schem/top.sym
** sch_path: tia_post_approval/schem/top.sch
.subckt top Iin_p Iin_n Vb1_ Vb2 Vb3_ Vb4_ Vb5 VDD GND Vout_n Vout_p
*.iopin VDD
*.iopin GND
*.opin Vout_n
*.ipin Iin_n
*.ipin Iin_p
*.ipin Vb1_
*.opin Vout_p
*.ipin Vb2
*.ipin Vb3_
*.ipin Vb4_
*.ipin Vb5
XR6 Vinn pre_Vout_p GND sky130_fd_pr__res_xhigh_po W=1.41 L=53 mult=1 m=1
XR1 pre_Vout_n Vinp GND sky130_fd_pr__res_xhigh_po W=1.41 L=53 mult=1 m=1
XR3 Vcm2 pre_Vout_p GND sky130_fd_pr__res_xhigh_po W=1.41 L=35 mult=1 m=1
XR5 pre_Vout_n Vcm2 GND sky130_fd_pr__res_xhigh_po W=1.41 L=35 mult=1 m=1
XR4 Vop net1 GND sky130_fd_pr__res_xhigh_po W=1.41 L=1.41 mult=1 m=1
XR10 Von net2 GND sky130_fd_pr__res_xhigh_po W=1.41 L=1.41 mult=1 m=1
XR17 Vcm1 Von GND sky130_fd_pr__res_xhigh_po W=1.41 L=35 mult=1 m=1
XR18 Vop Vcm1 GND sky130_fd_pr__res_xhigh_po W=1.41 L=35 mult=1 m=1
x1 Vinn Vinp Vb2 Vb1 Vcmfb1 VDD GND Vop Von core
x2 Vop Von Vb2 Vb1 Vcmfb2 VDD GND pre_Vout_n pre_Vout_p core
X1 VDD GND pre_Vout_n pre_Vout_p Vout_n Vout_p Vb4 sf
x3 Vcm1 Vb5 Vb3 VDD GND Vcmfb1 cmfb
x4 Vcm2 Vb5 Vb3 VDD GND Vcmfb2 cmfb
x5 Vb1 Vb1_ GND mirror_1
x6 Vb3 Vb3_ GND mirror_3
x7 Vb4 Vb4_ GND mirror_4
XC3 net1 pre_Vout_n sky130_fd_pr__cap_mim_m3_1 W=7.75 L=7.75 MF=1 m=1
XC4 pre_Vout_n net1 sky130_fd_pr__cap_mim_m3_2 W=7.75 L=7.75 MF=1 m=1
XC1 net2 pre_Vout_p sky130_fd_pr__cap_mim_m3_1 W=7.75 L=7.75 MF=1 m=1
XC2 pre_Vout_p net2 sky130_fd_pr__cap_mim_m3_2 W=7.75 L=7.75 MF=1 m=1
XC5 Vinn Iin_n sky130_fd_pr__cap_mim_m3_1 W=61.2 L=61.2 MF=1 m=1
XC6 Iin_n Vinn sky130_fd_pr__cap_mim_m3_2 W=61.2 L=61.2 MF=1 m=1
XC7 Vinp Iin_p sky130_fd_pr__cap_mim_m3_1 W=61.2 L=61.2 MF=1 m=1
XC8 Iin_p Vinp sky130_fd_pr__cap_mim_m3_2 W=61.2 L=61.2 MF=1 m=1
XC9 Vcmfb1 GND sky130_fd_pr__cap_mim_m3_1 W=33.5 L=33.5 MF=1 m=1
XC10 GND Vcmfb1 sky130_fd_pr__cap_mim_m3_2 W=33.5 L=33.5 MF=1 m=1
XC11 Vcmfb2 GND sky130_fd_pr__cap_mim_m3_1 W=33.5 L=33.5 MF=1 m=1
XC12 GND Vcmfb2 sky130_fd_pr__cap_mim_m3_2 W=33.5 L=33.5 MF=1 m=1
.ends


* expanding   symbol:  tia_post_approval/schem/core.sym # of pins=9
** sym_path: tia_post_approval/schem/core.sym
** sch_path: tia_post_approval/schem/core.sch
.subckt core Vin_n Vin_p Vb2 Vb1 Vcmfb VDD GND Vout_p Vout_n
*.ipin Vb2
*.ipin Vcmfb
*.iopin VDD
*.iopin GND
*.opin Vout_p
*.ipin Vin_p
*.ipin Vin_n
*.opin Vout_n
*.ipin Vb1
XM1 net1 Vb1 GND GND sky130_fd_pr__nfet_01v8 L=.5 W=710 nf=8 ad='int((nf+1)/2) * W/nf * 0.29' as='int((nf+2)/2) * W/nf * 0.29'
+ pd='2*int((nf+1)/2) * (W/nf + 0.29)' ps='2*int((nf+2)/2) * (W/nf + 0.29)' nrd='0.29 / W' nrs='0.29 / W'
+ sa=0 sb=0 sd=0 mult=1 m=1
x1 Vin_p Vb2 Vcmfb VDD GND Vout_n net1 core_half
x2 Vin_n Vb2 Vcmfb VDD GND Vout_p net1 core_half
.ends


* expanding   symbol:  tia_post_approval/schem/sf.sym # of pins=7
** sym_path: tia_post_approval/schem/sf.sym
** sch_path: tia_post_approval/schem/sf.sch
.subckt sf VDD GND Vin_p Vin_n Vout_p Vout_n Vb4
*.ipin Vin_n
*.iopin VDD
*.iopin GND
*.ipin Vin_p
*.opin Vout_n
*.opin Vout_p
*.iopin Vb4
X1 VDD Vb4 Vout_p Vin_p GND sf_half
X2 VDD Vb4 Vout_n Vin_n GND sf_half
.ends


* expanding   symbol:  tia_post_approval/schem/cmfb.sym # of pins=6
** sym_path: tia_post_approval/schem/cmfb.sym
** sch_path: tia_post_approval/schem/cmfb.sch
.subckt cmfb Vcm Vref Vb3 VDD GND Vcmfb
*.iopin VDD
*.iopin GND
*.opin Vcmfb
*.ipin Vref
*.iopin Vb3
*.ipin Vcm
x1 Vref net2 VDD GND Vb3 net3 Vcmfb cmfb_half
x2 Vcm net1 VDD GND Vb3 net3 net3 cmfb_half
XR20 net2 net1 GND sky130_fd_pr__res_xhigh_po W=1.41 L=1.41 mult=1 m=1
.ends


* expanding   symbol:  tia_post_approval/schem/mirror_1.sym # of pins=3
** sym_path: tia_post_approval/schem/mirror_1.sym
** sch_path: tia_post_approval/schem/mirror_1.sch
.subckt mirror_1 Vb1 Vb1_ GND
*.iopin GND
*.iopin Vb1_
*.opin Vb1
XM27 Vb1_ Vb1_ GND GND sky130_fd_pr__nfet_01v8 L=.5 W=3.6 nf=1 ad='int((nf+1)/2) * W/nf * 0.29' as='int((nf+2)/2) * W/nf * 0.29'
+ pd='2*int((nf+1)/2) * (W/nf + 0.29)' ps='2*int((nf+2)/2) * (W/nf + 0.29)' nrd='0.29 / W' nrs='0.29 / W'
+ sa=0 sb=0 sd=0 mult=1 m=1
XC1 Vb1 GND sky130_fd_pr__cap_mim_m3_1 W=15.8 L=15.8 MF=1 m=1
XC2 GND Vb1 sky130_fd_pr__cap_mim_m3_2 W=15.8 L=15.8 MF=1 m=1
XR11 V10 Vb1 GND sky130_fd_pr__res_xhigh_po W=0.35 L=16 mult=1 m=1
XR1 Vb1_ V1 GND sky130_fd_pr__res_xhigh_po W=0.35 L=16 mult=1 m=1
XR2 V10 V9 GND sky130_fd_pr__res_xhigh_po W=0.35 L=16 mult=1 m=1
XR3 V2 V1 GND sky130_fd_pr__res_xhigh_po W=0.35 L=16 mult=1 m=1
XR4 V8 V9 GND sky130_fd_pr__res_xhigh_po W=0.35 L=16 mult=1 m=1
XR5 V2 V3 GND sky130_fd_pr__res_xhigh_po W=0.35 L=16 mult=1 m=1
XR6 V8 V7 GND sky130_fd_pr__res_xhigh_po W=0.35 L=16 mult=1 m=1
XR7 V4 V3 GND sky130_fd_pr__res_xhigh_po W=0.35 L=16 mult=1 m=1
XR8 V6 V7 GND sky130_fd_pr__res_xhigh_po W=0.35 L=16 mult=1 m=1
XR9 V4 V5 GND sky130_fd_pr__res_xhigh_po W=0.35 L=16 mult=1 m=1
XR10 V6 V5 GND sky130_fd_pr__res_xhigh_po W=0.35 L=16 mult=1 m=1
XM1 GND GND Vb1_ GND sky130_fd_pr__nfet_01v8 L=.5 W=3.6 nf=1 ad='int((nf+1)/2) * W/nf * 0.29' as='int((nf+2)/2) * W/nf * 0.29'
+ pd='2*int((nf+1)/2) * (W/nf + 0.29)' ps='2*int((nf+2)/2) * (W/nf + 0.29)' nrd='0.29 / W' nrs='0.29 / W'
+ sa=0 sb=0 sd=0 mult=1 m=1
XM2 GND GND GND GND sky130_fd_pr__nfet_01v8 L=.5 W=3.6 nf=1 ad='int((nf+1)/2) * W/nf * 0.29' as='int((nf+2)/2) * W/nf * 0.29'
+ pd='2*int((nf+1)/2) * (W/nf + 0.29)' ps='2*int((nf+2)/2) * (W/nf + 0.29)' nrd='0.29 / W' nrs='0.29 / W'
+ sa=0 sb=0 sd=0 mult=1 m=1
.ends


* expanding   symbol:  tia_post_approval/schem/mirror_3.sym # of pins=3
** sym_path: tia_post_approval/schem/mirror_3.sym
** sch_path: tia_post_approval/schem/mirror_3.sch
.subckt mirror_3 Vb3 Vb3_ GND
*.iopin GND
*.iopin Vb3_
*.opin Vb3
XM27 Vb3_ Vb3_ GND GND sky130_fd_pr__nfet_01v8 L=.5 W=5 nf=1 ad='int((nf+1)/2) * W/nf * 0.29' as='int((nf+2)/2) * W/nf * 0.29'
+ pd='2*int((nf+1)/2) * (W/nf + 0.29)' ps='2*int((nf+2)/2) * (W/nf + 0.29)' nrd='0.29 / W' nrs='0.29 / W'
+ sa=0 sb=0 sd=0 mult=2 m=2
XR11 V10 Vb3 GND sky130_fd_pr__res_xhigh_po W=0.35 L=16 mult=1 m=1
XC1 Vb3 GND sky130_fd_pr__cap_mim_m3_1 W=15.8 L=15.8 MF=1 m=1
XC2 GND Vb3 sky130_fd_pr__cap_mim_m3_2 W=15.8 L=15.8 MF=1 m=1
XR1 Vb3_ V1 GND sky130_fd_pr__res_xhigh_po W=0.35 L=16 mult=1 m=1
XR2 V10 V9 GND sky130_fd_pr__res_xhigh_po W=0.35 L=16 mult=1 m=1
XR3 V2 V1 GND sky130_fd_pr__res_xhigh_po W=0.35 L=16 mult=1 m=1
XR4 V8 V9 GND sky130_fd_pr__res_xhigh_po W=0.35 L=16 mult=1 m=1
XR5 V2 V3 GND sky130_fd_pr__res_xhigh_po W=0.35 L=16 mult=1 m=1
XR6 V8 V7 GND sky130_fd_pr__res_xhigh_po W=0.35 L=16 mult=1 m=1
XR7 V4 V3 GND sky130_fd_pr__res_xhigh_po W=0.35 L=16 mult=1 m=1
XR8 V6 V7 GND sky130_fd_pr__res_xhigh_po W=0.35 L=16 mult=1 m=1
XR9 V4 V5 GND sky130_fd_pr__res_xhigh_po W=0.35 L=16 mult=1 m=1
XR10 V6 V5 GND sky130_fd_pr__res_xhigh_po W=0.35 L=16 mult=1 m=1
.ends


* expanding   symbol:  tia_post_approval/schem/mirror_4.sym # of pins=3
** sym_path: tia_post_approval/schem/mirror_4.sym
** sch_path: tia_post_approval/schem/mirror_4.sch
.subckt mirror_4 Vb4 Vb4_ GND
*.iopin GND
*.iopin Vb4_
*.opin Vb4
XM27 Vb4_ Vb4_ GND GND sky130_fd_pr__nfet_01v8 L=.45 W=4 nf=1 ad='int((nf+1)/2) * W/nf * 0.29' as='int((nf+2)/2) * W/nf * 0.29'
+ pd='2*int((nf+1)/2) * (W/nf + 0.29)' ps='2*int((nf+2)/2) * (W/nf + 0.29)' nrd='0.29 / W' nrs='0.29 / W'
+ sa=0 sb=0 sd=0 mult=1 m=1
XC1 Vb4 GND sky130_fd_pr__cap_mim_m3_1 W=15.8 L=15.8 MF=1 m=1
XC2 GND Vb4 sky130_fd_pr__cap_mim_m3_2 W=15.8 L=15.8 MF=1 m=1
XR11 V10 Vb4 GND sky130_fd_pr__res_xhigh_po W=0.35 L=16 mult=1 m=1
XR1 Vb4_ V1 GND sky130_fd_pr__res_xhigh_po W=0.35 L=16 mult=1 m=1
XR2 V10 V9 GND sky130_fd_pr__res_xhigh_po W=0.35 L=16 mult=1 m=1
XR3 V2 V1 GND sky130_fd_pr__res_xhigh_po W=0.35 L=16 mult=1 m=1
XR4 V8 V9 GND sky130_fd_pr__res_xhigh_po W=0.35 L=16 mult=1 m=1
XR5 V2 V3 GND sky130_fd_pr__res_xhigh_po W=0.35 L=16 mult=1 m=1
XR6 V8 V7 GND sky130_fd_pr__res_xhigh_po W=0.35 L=16 mult=1 m=1
XR7 V4 V3 GND sky130_fd_pr__res_xhigh_po W=0.35 L=16 mult=1 m=1
XR8 V6 V7 GND sky130_fd_pr__res_xhigh_po W=0.35 L=16 mult=1 m=1
XR9 V4 V5 GND sky130_fd_pr__res_xhigh_po W=0.35 L=16 mult=1 m=1
XR10 V6 V5 GND sky130_fd_pr__res_xhigh_po W=0.35 L=16 mult=1 m=1
.ends


* expanding   symbol:  tia_post_approval/schem/core_half.sym # of pins=7
** sym_path: tia_post_approval/schem/core_half.sym
** sch_path: tia_post_approval/schem/core_half.sch
.subckt core_half Vin Vb2 Vcmfb VDD GND Vout s
*.ipin Vb2
*.ipin Vcmfb
*.iopin VDD
*.iopin GND
*.opin Vout
*.iopin s
*.ipin Vin
XM3 Vout Vin s GND sky130_fd_pr__nfet_01v8 L=0.15 W=150 nf=4 ad='int((nf+1)/2) * W/nf * 0.29' as='int((nf+2)/2) * W/nf * 0.29'
+ pd='2*int((nf+1)/2) * (W/nf + 0.29)' ps='2*int((nf+2)/2) * (W/nf + 0.29)' nrd='0.29 / W' nrs='0.29 / W'
+ sa=0 sb=0 sd=0 mult=1 m=1
XM5 Vout Vcmfb VDD VDD sky130_fd_pr__pfet_01v8 L=0.18 W=112 nf=5 ad='int((nf+1)/2) * W/nf * 0.29' as='int((nf+2)/2) * W/nf * 0.29'
+ pd='2*int((nf+1)/2) * (W/nf + 0.29)' ps='2*int((nf+2)/2) * (W/nf + 0.29)' nrd='0.29 / W' nrs='0.29 / W'
+ sa=0 sb=0 sd=0 mult=1 m=1
XM25 Vout Vb2 VDD VDD sky130_fd_pr__pfet_01v8 L=0.18 W=448 nf=15 ad='int((nf+1)/2) * W/nf * 0.29' as='int((nf+2)/2) * W/nf * 0.29'
+ pd='2*int((nf+1)/2) * (W/nf + 0.29)' ps='2*int((nf+2)/2) * (W/nf + 0.29)' nrd='0.29 / W' nrs='0.29 / W'
+ sa=0 sb=0 sd=0 mult=1 m=1
.ends


* expanding   symbol:  tia_post_approval/schem/sf_half.sym # of pins=5
** sym_path: tia_post_approval/schem/sf_half.sym
** sch_path: tia_post_approval/schem/sf_half.sch
.subckt sf_half VDD g_d Vout g_u GND
*.iopin VDD
*.iopin g_u
*.iopin GND
*.iopin Vout
*.iopin g_d
XM17 VDD g_u Vout GND sky130_fd_pr__nfet_01v8_lvt L=0.32 W=650 nf=26 ad='int((nf+1)/2) * W/nf * 0.29'
+ as='int((nf+2)/2) * W/nf * 0.29' pd='2*int((nf+1)/2) * (W/nf + 0.29)' ps='2*int((nf+2)/2) * (W/nf + 0.29)'
+ nrd='0.29 / W' nrs='0.29 / W' sa=0 sb=0 sd=0 mult=1 m=1
XM19 Vout g_d GND GND sky130_fd_pr__nfet_01v8 L=.45 W=650 nf=26 ad='int((nf+1)/2) * W/nf * 0.29' as='int((nf+2)/2) * W/nf * 0.29'
+ pd='2*int((nf+1)/2) * (W/nf + 0.29)' ps='2*int((nf+2)/2) * (W/nf + 0.29)' nrd='0.29 / W' nrs='0.29 / W'
+ sa=0 sb=0 sd=0 mult=1 m=1
.ends


* expanding   symbol:  tia_post_approval/schem/cmfb_half.sym # of pins=7
** sym_path: tia_post_approval/schem/cmfb_half.sym
** sch_path: tia_post_approval/schem/cmfb_half.sch
.subckt cmfb_half Vin res VDD GND Vb3 diode Vout
*.iopin VDD
*.iopin GND
*.opin Vout
*.ipin Vin
*.iopin diode
*.iopin Vb3
*.iopin res
XM11 Vout Vin res GND sky130_fd_pr__nfet_01v8 L=0.20 W=150 nf=2 ad='int((nf+1)/2) * W/nf * 0.29' as='int((nf+2)/2) * W/nf * 0.29'
+ pd='2*int((nf+1)/2) * (W/nf + 0.29)' ps='2*int((nf+2)/2) * (W/nf + 0.29)' nrd='0.29 / W' nrs='0.29 / W'
+ sa=0 sb=0 sd=0 mult=1 m=1
XM14 Vout diode VDD VDD sky130_fd_pr__pfet_01v8 L=0.2 W=42 nf=1 ad='int((nf+1)/2) * W/nf * 0.29' as='int((nf+2)/2) * W/nf * 0.29'
+ pd='2*int((nf+1)/2) * (W/nf + 0.29)' ps='2*int((nf+2)/2) * (W/nf + 0.29)' nrd='0.29 / W' nrs='0.29 / W'
+ sa=0 sb=0 sd=0 mult=1 m=1
XM15 res Vb3 GND GND sky130_fd_pr__nfet_01v8 L=.5 W=65 nf=1 ad='int((nf+1)/2) * W/nf * 0.29' as='int((nf+2)/2) * W/nf * 0.29'
+ pd='2*int((nf+1)/2) * (W/nf + 0.29)' ps='2*int((nf+2)/2) * (W/nf + 0.29)' nrd='0.29 / W' nrs='0.29 / W'
+ sa=0 sb=0 sd=0 mult=1 m=1
.ends

.GLOBAL GND
.end
